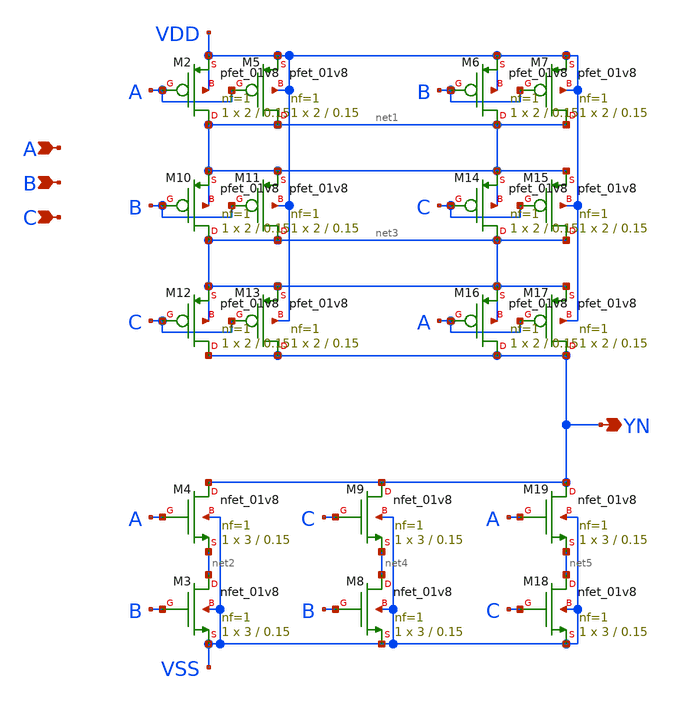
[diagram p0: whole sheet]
** sch_path: lib/xschem/VOTERN3X1.sch
**.subckt VOTERN3X1 A YN B C
*.ipin A
*.opin YN
*.ipin B
*.ipin C
XM2 net1 A VDD VDD sky130_fd_pr__pfet_01v8 L=0.15 W=2 nf=1 ad='int((nf+1)/2) * W/nf * 0.29' as='int((nf+2)/2) * W/nf * 0.29'
+ pd='2*int((nf+1)/2) * (W/nf + 0.29)' ps='2*int((nf+2)/2) * (W/nf + 0.29)' nrd='0.29 / W' nrs='0.29 / W'
+ sa=0 sb=0 sd=0 mult=1 m=1
XM3 net2 B VSS VSS sky130_fd_pr__nfet_01v8 L=0.15 W=3 nf=1 ad='int((nf+1)/2) * W/nf * 0.29' as='int((nf+2)/2) * W/nf * 0.29'
+ pd='2*int((nf+1)/2) * (W/nf + 0.29)' ps='2*int((nf+2)/2) * (W/nf + 0.29)' nrd='0.29 / W' nrs='0.29 / W'
+ sa=0 sb=0 sd=0 mult=1 m=1
XM4 YN A net2 VSS sky130_fd_pr__nfet_01v8 L=0.15 W=3 nf=1 ad='int((nf+1)/2) * W/nf * 0.29' as='int((nf+2)/2) * W/nf * 0.29'
+ pd='2*int((nf+1)/2) * (W/nf + 0.29)' ps='2*int((nf+2)/2) * (W/nf + 0.29)' nrd='0.29 / W' nrs='0.29 / W'
+ sa=0 sb=0 sd=0 mult=1 m=1
XM5 net1 A VDD VDD sky130_fd_pr__pfet_01v8 L=0.15 W=2 nf=1 ad='int((nf+1)/2) * W/nf * 0.29' as='int((nf+2)/2) * W/nf * 0.29'
+ pd='2*int((nf+1)/2) * (W/nf + 0.29)' ps='2*int((nf+2)/2) * (W/nf + 0.29)' nrd='0.29 / W' nrs='0.29 / W'
+ sa=0 sb=0 sd=0 mult=1 m=1
XM6 net1 B VDD VDD sky130_fd_pr__pfet_01v8 L=0.15 W=2 nf=1 ad='int((nf+1)/2) * W/nf * 0.29' as='int((nf+2)/2) * W/nf * 0.29'
+ pd='2*int((nf+1)/2) * (W/nf + 0.29)' ps='2*int((nf+2)/2) * (W/nf + 0.29)' nrd='0.29 / W' nrs='0.29 / W'
+ sa=0 sb=0 sd=0 mult=1 m=1
XM7 net1 B VDD VDD sky130_fd_pr__pfet_01v8 L=0.15 W=2 nf=1 ad='int((nf+1)/2) * W/nf * 0.29' as='int((nf+2)/2) * W/nf * 0.29'
+ pd='2*int((nf+1)/2) * (W/nf + 0.29)' ps='2*int((nf+2)/2) * (W/nf + 0.29)' nrd='0.29 / W' nrs='0.29 / W'
+ sa=0 sb=0 sd=0 mult=1 m=1
XM10 net3 B net1 net1 sky130_fd_pr__pfet_01v8 L=0.15 W=2 nf=1 ad='int((nf+1)/2) * W/nf * 0.29' as='int((nf+2)/2) * W/nf * 0.29'
+ pd='2*int((nf+1)/2) * (W/nf + 0.29)' ps='2*int((nf+2)/2) * (W/nf + 0.29)' nrd='0.29 / W' nrs='0.29 / W'
+ sa=0 sb=0 sd=0 mult=1 m=1
XM11 net3 B net1 VDD sky130_fd_pr__pfet_01v8 L=0.15 W=2 nf=1 ad='int((nf+1)/2) * W/nf * 0.29' as='int((nf+2)/2) * W/nf * 0.29'
+ pd='2*int((nf+1)/2) * (W/nf + 0.29)' ps='2*int((nf+2)/2) * (W/nf + 0.29)' nrd='0.29 / W' nrs='0.29 / W'
+ sa=0 sb=0 sd=0 mult=1 m=1
XM12 YN C net3 net3 sky130_fd_pr__pfet_01v8 L=0.15 W=2 nf=1 ad='int((nf+1)/2) * W/nf * 0.29' as='int((nf+2)/2) * W/nf * 0.29'
+ pd='2*int((nf+1)/2) * (W/nf + 0.29)' ps='2*int((nf+2)/2) * (W/nf + 0.29)' nrd='0.29 / W' nrs='0.29 / W'
+ sa=0 sb=0 sd=0 mult=1 m=1
XM13 YN C net3 VDD sky130_fd_pr__pfet_01v8 L=0.15 W=2 nf=1 ad='int((nf+1)/2) * W/nf * 0.29' as='int((nf+2)/2) * W/nf * 0.29'
+ pd='2*int((nf+1)/2) * (W/nf + 0.29)' ps='2*int((nf+2)/2) * (W/nf + 0.29)' nrd='0.29 / W' nrs='0.29 / W'
+ sa=0 sb=0 sd=0 mult=1 m=1
XM14 net3 C net1 net1 sky130_fd_pr__pfet_01v8 L=0.15 W=2 nf=1 ad='int((nf+1)/2) * W/nf * 0.29' as='int((nf+2)/2) * W/nf * 0.29'
+ pd='2*int((nf+1)/2) * (W/nf + 0.29)' ps='2*int((nf+2)/2) * (W/nf + 0.29)' nrd='0.29 / W' nrs='0.29 / W'
+ sa=0 sb=0 sd=0 mult=1 m=1
XM15 net3 C net1 VDD sky130_fd_pr__pfet_01v8 L=0.15 W=2 nf=1 ad='int((nf+1)/2) * W/nf * 0.29' as='int((nf+2)/2) * W/nf * 0.29'
+ pd='2*int((nf+1)/2) * (W/nf + 0.29)' ps='2*int((nf+2)/2) * (W/nf + 0.29)' nrd='0.29 / W' nrs='0.29 / W'
+ sa=0 sb=0 sd=0 mult=1 m=1
XM16 YN A net3 net3 sky130_fd_pr__pfet_01v8 L=0.15 W=2 nf=1 ad='int((nf+1)/2) * W/nf * 0.29' as='int((nf+2)/2) * W/nf * 0.29'
+ pd='2*int((nf+1)/2) * (W/nf + 0.29)' ps='2*int((nf+2)/2) * (W/nf + 0.29)' nrd='0.29 / W' nrs='0.29 / W'
+ sa=0 sb=0 sd=0 mult=1 m=1
XM17 YN A net3 VDD sky130_fd_pr__pfet_01v8 L=0.15 W=2 nf=1 ad='int((nf+1)/2) * W/nf * 0.29' as='int((nf+2)/2) * W/nf * 0.29'
+ pd='2*int((nf+1)/2) * (W/nf + 0.29)' ps='2*int((nf+2)/2) * (W/nf + 0.29)' nrd='0.29 / W' nrs='0.29 / W'
+ sa=0 sb=0 sd=0 mult=1 m=1
XM8 net4 B VSS VSS sky130_fd_pr__nfet_01v8 L=0.15 W=3 nf=1 ad='int((nf+1)/2) * W/nf * 0.29' as='int((nf+2)/2) * W/nf * 0.29'
+ pd='2*int((nf+1)/2) * (W/nf + 0.29)' ps='2*int((nf+2)/2) * (W/nf + 0.29)' nrd='0.29 / W' nrs='0.29 / W'
+ sa=0 sb=0 sd=0 mult=1 m=1
XM9 YN C net4 VSS sky130_fd_pr__nfet_01v8 L=0.15 W=3 nf=1 ad='int((nf+1)/2) * W/nf * 0.29' as='int((nf+2)/2) * W/nf * 0.29'
+ pd='2*int((nf+1)/2) * (W/nf + 0.29)' ps='2*int((nf+2)/2) * (W/nf + 0.29)' nrd='0.29 / W' nrs='0.29 / W'
+ sa=0 sb=0 sd=0 mult=1 m=1
XM18 net5 C VSS VSS sky130_fd_pr__nfet_01v8 L=0.15 W=3 nf=1 ad='int((nf+1)/2) * W/nf * 0.29' as='int((nf+2)/2) * W/nf * 0.29'
+ pd='2*int((nf+1)/2) * (W/nf + 0.29)' ps='2*int((nf+2)/2) * (W/nf + 0.29)' nrd='0.29 / W' nrs='0.29 / W'
+ sa=0 sb=0 sd=0 mult=1 m=1
XM19 YN A net5 VSS sky130_fd_pr__nfet_01v8 L=0.15 W=3 nf=1 ad='int((nf+1)/2) * W/nf * 0.29' as='int((nf+2)/2) * W/nf * 0.29'
+ pd='2*int((nf+1)/2) * (W/nf + 0.29)' ps='2*int((nf+2)/2) * (W/nf + 0.29)' nrd='0.29 / W' nrs='0.29 / W'
+ sa=0 sb=0 sd=0 mult=1 m=1
**.ends
.end
